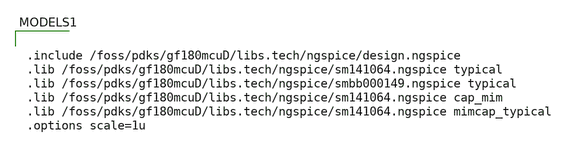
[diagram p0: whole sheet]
** sch_path: activities/opamp1Aysha/randomIgnore.sch
**.subckt randomIgnore
**** begin user architecture code


.include /foss/pdks/gf180mcuD/libs.tech/ngspice/design.ngspice
.lib /foss/pdks/gf180mcuD/libs.tech/ngspice/sm141064.ngspice typical
.lib /foss/pdks/gf180mcuD/libs.tech/ngspice/smbb000149.ngspice typical
.lib /foss/pdks/gf180mcuD/libs.tech/ngspice/sm141064.ngspice cap_mim
.lib /foss/pdks/gf180mcuD/libs.tech/ngspice/sm141064.ngspice mimcap_typical
.options scale=1u


**** end user architecture code
**.ends
.end
